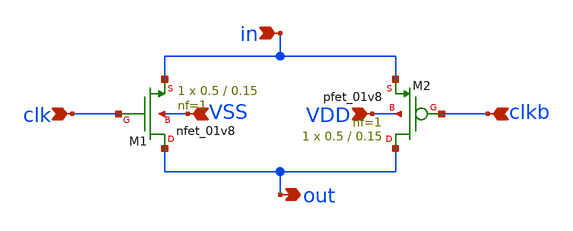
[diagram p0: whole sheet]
** sch_path: transmission_gate.sch
**.subckt transmission_gate in clk clkb out VDD VSS
*.ipin in
*.ipin clk
*.ipin clkb
*.opin out
*.ipin VDD
*.ipin VSS
XM1 out clk in VSS sky130_fd_pr__nfet_01v8 L=0.15 W=0.5 nf=1 ad='int((nf+1)/2) * W/nf * 0.29' as='int((nf+2)/2) * W/nf * 0.29'
+ pd='2*int((nf+1)/2) * (W/nf + 0.29)' ps='2*int((nf+2)/2) * (W/nf + 0.29)' nrd='0.29 / W' nrs='0.29 / W'
+ sa=0 sb=0 sd=0 mult=1 m=1
XM2 out clkb in VDD sky130_fd_pr__pfet_01v8 L=0.15 W=0.5 nf=1 ad='int((nf+1)/2) * W/nf * 0.29' as='int((nf+2)/2) * W/nf * 0.29'
+ pd='2*int((nf+1)/2) * (W/nf + 0.29)' ps='2*int((nf+2)/2) * (W/nf + 0.29)' nrd='0.29 / W' nrs='0.29 / W'
+ sa=0 sb=0 sd=0 mult=1 m=1
**.ends
.end
